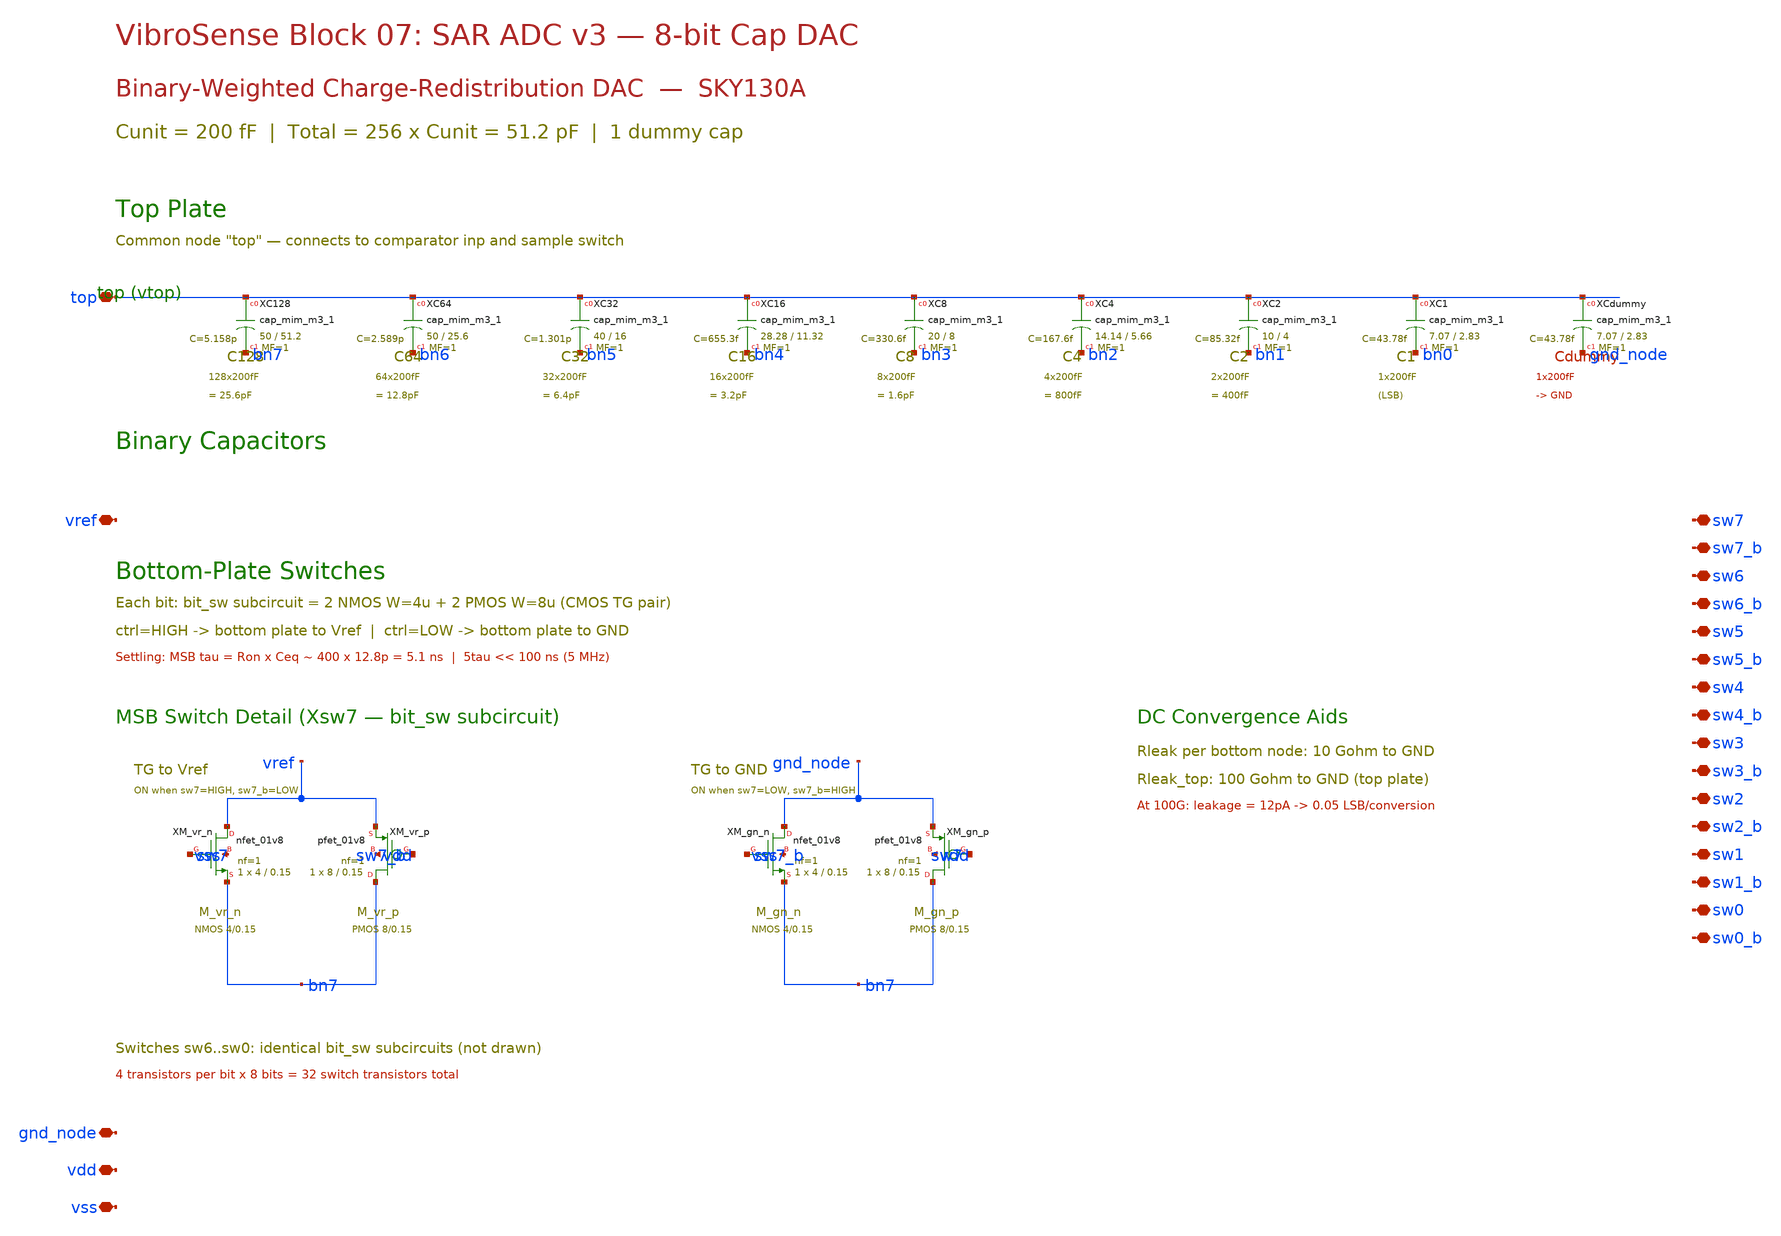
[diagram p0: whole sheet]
** sch_path: vibrosense/07_adc_v3/v3_cap_dac.sch
**.subckt v3_cap_dac top vref gnd_node vdd vss sw7 sw7_b sw6 sw6_b sw5 sw5_b sw4 sw4_b sw3 sw3_b sw2
*+ sw2_b sw1 sw1_b sw0 sw0_b
*.iopin top
*.iopin vref
*.iopin gnd_node
*.iopin vdd
*.iopin vss
*.iopin sw7
*.iopin sw7_b
*.iopin sw6
*.iopin sw6_b
*.iopin sw5
*.iopin sw5_b
*.iopin sw4
*.iopin sw4_b
*.iopin sw3
*.iopin sw3_b
*.iopin sw2
*.iopin sw2_b
*.iopin sw1
*.iopin sw1_b
*.iopin sw0
*.iopin sw0_b
XXC128 top bn7 sky130_fd_pr__cap_mim_m3_1 W=50 L=51.2 MF=1 m=1
XXC64 top bn6 sky130_fd_pr__cap_mim_m3_1 W=50 L=25.6 MF=1 m=1
XXC32 top bn5 sky130_fd_pr__cap_mim_m3_1 W=40 L=16 MF=1 m=1
XXC16 top bn4 sky130_fd_pr__cap_mim_m3_1 W=28.28 L=11.32 MF=1 m=1
XXC8 top bn3 sky130_fd_pr__cap_mim_m3_1 W=20 L=8 MF=1 m=1
XXC4 top bn2 sky130_fd_pr__cap_mim_m3_1 W=14.14 L=5.66 MF=1 m=1
XXC2 top bn1 sky130_fd_pr__cap_mim_m3_1 W=10 L=4 MF=1 m=1
XXC1 top bn0 sky130_fd_pr__cap_mim_m3_1 W=7.07 L=2.83 MF=1 m=1
XXCdummy top gnd_node sky130_fd_pr__cap_mim_m3_1 W=7.07 L=2.83 MF=1 m=1
XXM_vr_n vref sw7 bn7 vss sky130_fd_pr__nfet_01v8 L=0.15 W=4 nf=1 ad='int((1 + 1)/2) * 4 / 1 * 0.29'
+ as='int((1 + 2)/2) * 4 / 1 * 0.29' pd='2*int((1 + 1)/2) * (4 / 1 + 0.29)' ps='2*int((1 + 2)/2) * (4 / 1 + 0.29)'
+ nrd='0.29 / 4 ' nrs='0.29 / 4 ' sa=0 sb=0 sd=0 mult=1 m=1
XXM_vr_p bn7 sw7_b vref vdd sky130_fd_pr__pfet_01v8 L=0.15 W=8 nf=1 ad='int((nf+1)/2) * W/nf * 0.29'
+ as='int((nf+2)/2) * W/nf * 0.29' pd='2*int((nf+1)/2) * (W/nf + 0.29)' ps='2*int((nf+2)/2) * (W/nf + 0.29)'
+ nrd='0.29 / W' nrs='0.29 / W' sa=0 sb=0 sd=0 mult=1 m=1
XXM_gn_n gnd_node sw7_b bn7 vss sky130_fd_pr__nfet_01v8 L=0.15 W=4 nf=1 ad='int((1 + 1)/2) * 4 / 1 * 0.29'
+ as='int((1 + 2)/2) * 4 / 1 * 0.29' pd='2*int((1 + 1)/2) * (4 / 1 + 0.29)' ps='2*int((1 + 2)/2) * (4 / 1 + 0.29)'
+ nrd='0.29 / 4 ' nrs='0.29 / 4 ' sa=0 sb=0 sd=0 mult=1 m=1
XXM_gn_p bn7 sw7 gnd_node vdd sky130_fd_pr__pfet_01v8 L=0.15 W=8 nf=1 ad='int((nf+1)/2) * W/nf * 0.29'
+ as='int((nf+2)/2) * W/nf * 0.29' pd='2*int((nf+1)/2) * (W/nf + 0.29)' ps='2*int((nf+2)/2) * (W/nf + 0.29)'
+ nrd='0.29 / W' nrs='0.29 / W' sa=0 sb=0 sd=0 mult=1 m=1
**.ends
.end
